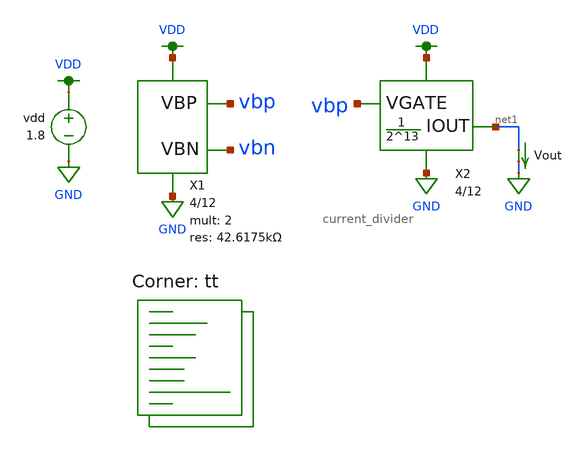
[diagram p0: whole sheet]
** sch_path: dac/schematic/current_divider_tb.sch
**.subckt current_divider_tb
vdd VDD GND 1.8
X1 vbp VDD GND vbn bias_gen u_w=4 u_l=12 m=2 r=42.6175k
Vout net1 GND 0
.save i(vout)
X2 GND VDD net1 vbp current_divider u_w=4 u_l=12
**** begin user architecture code
.lib $::SKYWATER_MODELS/sky130.lib.spice tt

.ic v(vbp)=0 v(vbn)=0
.control
  set wr_vecnames
  set wr_singlescale
  op
  wrdata ~/documents/git/madvlsi/dac/build/current_divider/current_divider_tb.txt i(Vout)
.endc

**** end user architecture code
**.ends
.GLOBAL GND
.GLOBAL VDD
.end
